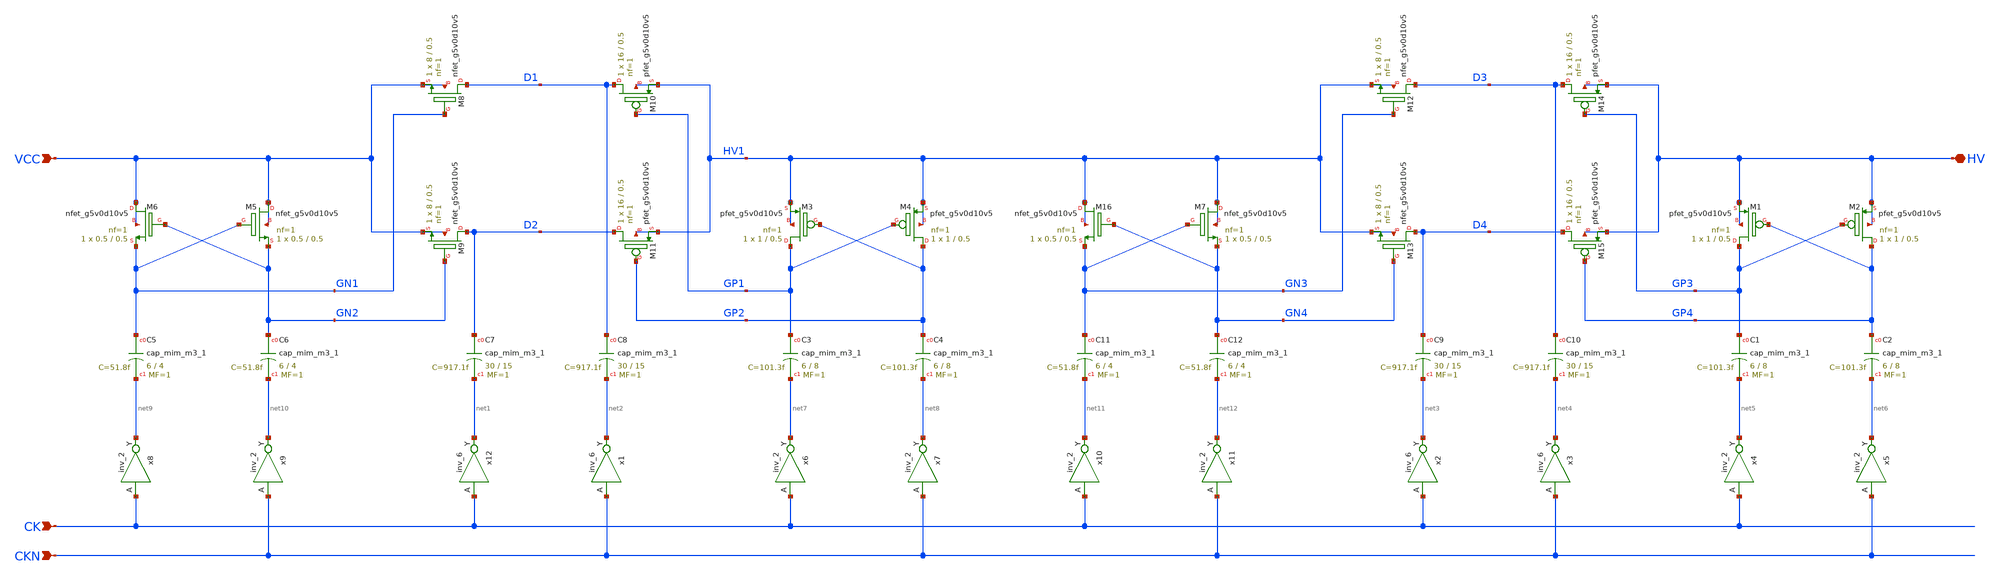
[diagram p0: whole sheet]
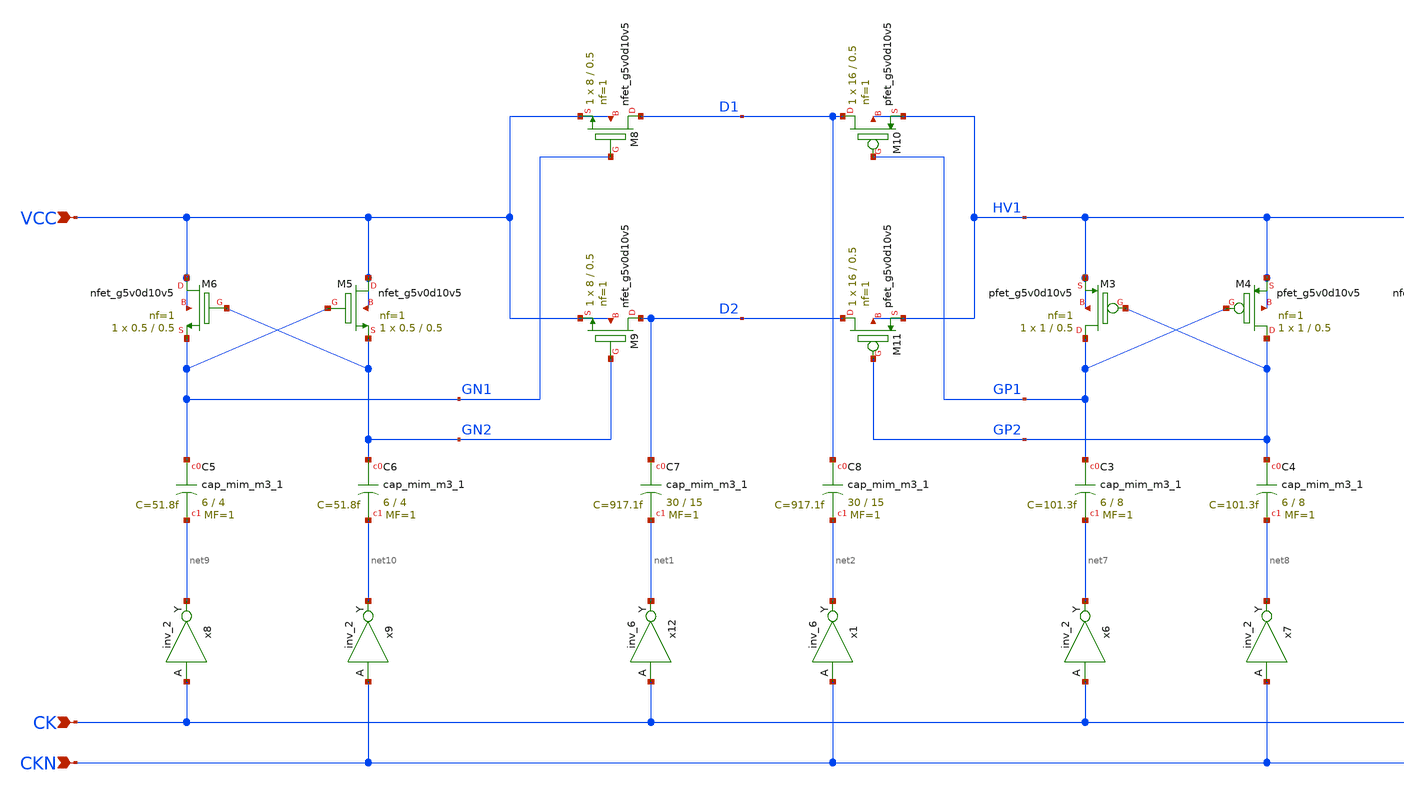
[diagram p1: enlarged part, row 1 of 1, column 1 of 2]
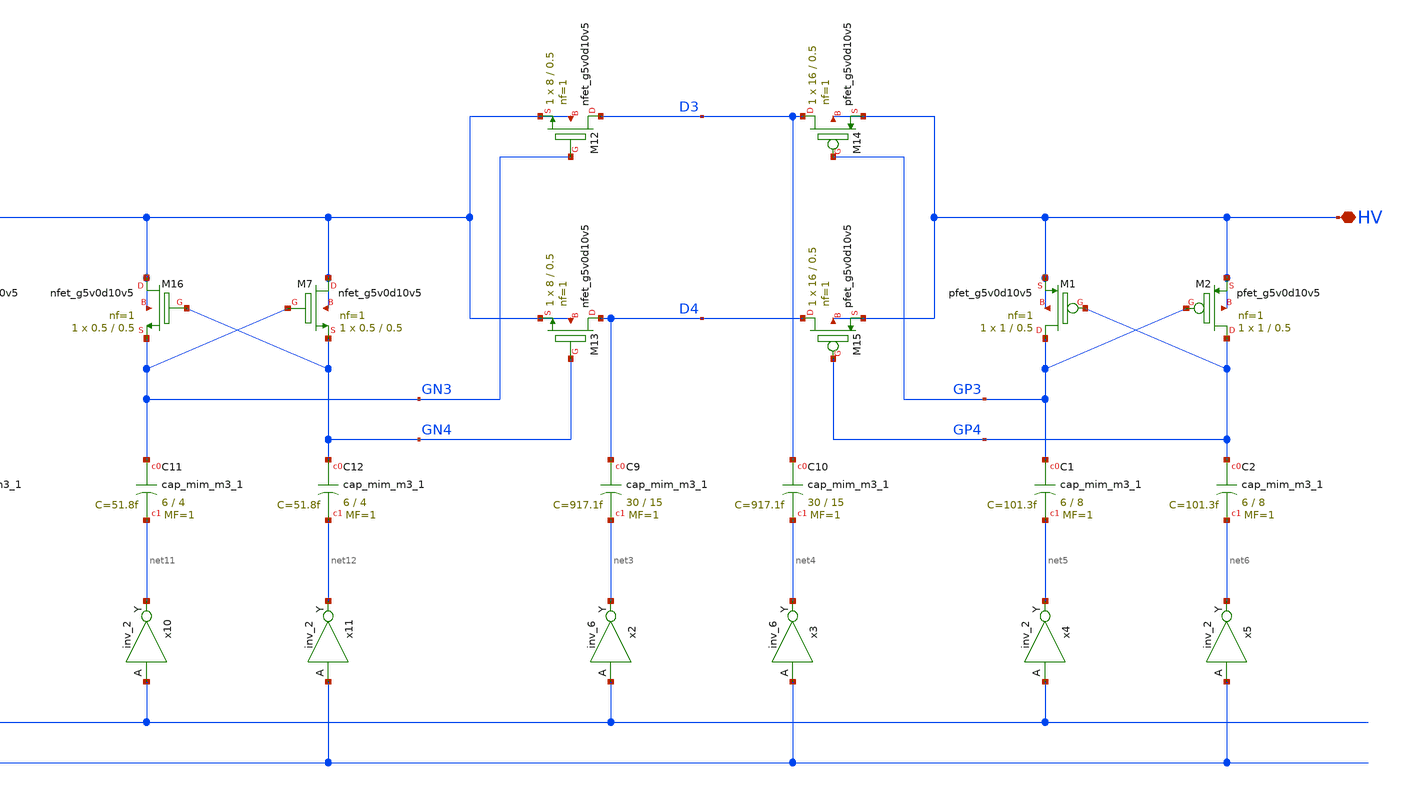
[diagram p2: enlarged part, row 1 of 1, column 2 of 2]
** sch_path: sky130A/xschem_libs/sky130_tests_ase/charge_pump2/schematic/charge_pump2.sch
* Copyright 2021 Stefan Frederik Schippers
* Licensed under the Apache License, Version 2.0 (the "License");
* you may not use this file except in compliance with the License.
* You may obtain a copy of the License at
* https://www.apache.org/licenses/LICENSE-2.0
* Unless required by applicable law or agreed to in writing, software
* distributed under the License is distributed on an "AS IS" BASIS,
* WITHOUT WARRANTIES OR CONDITIONS OF ANY KIND, either express or implied.
* See the License for the specific language governing permissions and
* limitations under the License.
**.subckt charge_pump2 VCC HV CK CKN
*.ipin VCC
*.iopin HV
*.ipin CK
*.ipin CKN
XM8 D1 GN1 VCC VCC sky130_fd_pr__nfet_g5v0d10v5 L=0.5 W=8 nf=1 ad='int((1 + 1)/2) * 8 / 1 * 0.29' as='int((1 + 2)/2) * 8 / 1 * 0.29'
+ pd='2*int((1 + 1)/2) * (8 / 1 + 0.29)' ps='2*int((1 + 2)/2) * (8 / 1 + 0.29)' nrd='0.29 / 8 ' nrs='0.29 / 8 '
+ sa=0 sb=0 sd=0 mult=1 m=1
XM9 D2 GN2 VCC VCC sky130_fd_pr__nfet_g5v0d10v5 L=0.5 W=8 nf=1 ad='int((1 + 1)/2) * 8 / 1 * 0.29' as='int((1 + 2)/2) * 8 / 1 * 0.29'
+ pd='2*int((1 + 1)/2) * (8 / 1 + 0.29)' ps='2*int((1 + 2)/2) * (8 / 1 + 0.29)' nrd='0.29 / 8 ' nrs='0.29 / 8 '
+ sa=0 sb=0 sd=0 mult=1 m=1
XM10 D1 GP1 HV1 HV1 sky130_fd_pr__pfet_g5v0d10v5 L=0.5 W=16 nf=1 ad='int((1 + 1)/2) * 16 / 1 * 0.29'
+ as='int((1 + 2)/2) * 16 / 1 * 0.29' pd='2*int((1 + 1)/2) * (16 / 1 + 0.29)' ps='2*int((1 + 2)/2) * (16 / 1 + 0.29)'
+ nrd='0.29 / 16 ' nrs='0.29 / 16 ' sa=0 sb=0 sd=0 mult=1 m=1
XM11 D2 GP2 HV1 HV1 sky130_fd_pr__pfet_g5v0d10v5 L=0.5 W=16 nf=1 ad='int((1 + 1)/2) * 16 / 1 * 0.29'
+ as='int((1 + 2)/2) * 16 / 1 * 0.29' pd='2*int((1 + 1)/2) * (16 / 1 + 0.29)' ps='2*int((1 + 2)/2) * (16 / 1 + 0.29)'
+ nrd='0.29 / 16 ' nrs='0.29 / 16 ' sa=0 sb=0 sd=0 mult=1 m=1
XC7 D2 net1 sky130_fd_pr__cap_mim_m3_1 W=30 L=15 MF=1 m=1
XC8 D1 net2 sky130_fd_pr__cap_mim_m3_1 W=30 L=15 MF=1 m=1
XM12 D3 GN3 HV1 HV1 sky130_fd_pr__nfet_g5v0d10v5 L=0.5 W=8 nf=1 ad='int((1 + 1)/2) * 8 / 1 * 0.29' as='int((1 + 2)/2) * 8 / 1 * 0.29'
+ pd='2*int((1 + 1)/2) * (8 / 1 + 0.29)' ps='2*int((1 + 2)/2) * (8 / 1 + 0.29)' nrd='0.29 / 8 ' nrs='0.29 / 8 '
+ sa=0 sb=0 sd=0 mult=1 m=1
XM13 D4 GN4 HV1 HV1 sky130_fd_pr__nfet_g5v0d10v5 L=0.5 W=8 nf=1 ad='int((1 + 1)/2) * 8 / 1 * 0.29' as='int((1 + 2)/2) * 8 / 1 * 0.29'
+ pd='2*int((1 + 1)/2) * (8 / 1 + 0.29)' ps='2*int((1 + 2)/2) * (8 / 1 + 0.29)' nrd='0.29 / 8 ' nrs='0.29 / 8 '
+ sa=0 sb=0 sd=0 mult=1 m=1
XM14 D3 GP3 HV HV sky130_fd_pr__pfet_g5v0d10v5 L=0.5 W=16 nf=1 ad='int((1 + 1)/2) * 16 / 1 * 0.29' as='int((1 + 2)/2) * 16 / 1 * 0.29'
+ pd='2*int((1 + 1)/2) * (16 / 1 + 0.29)' ps='2*int((1 + 2)/2) * (16 / 1 + 0.29)' nrd='0.29 / 16 ' nrs='0.29 / 16 '
+ sa=0 sb=0 sd=0 mult=1 m=1
XM15 D4 GP4 HV HV sky130_fd_pr__pfet_g5v0d10v5 L=0.5 W=16 nf=1 ad='int((1 + 1)/2) * 16 / 1 * 0.29' as='int((1 + 2)/2) * 16 / 1 * 0.29'
+ pd='2*int((1 + 1)/2) * (16 / 1 + 0.29)' ps='2*int((1 + 2)/2) * (16 / 1 + 0.29)' nrd='0.29 / 16 ' nrs='0.29 / 16 '
+ sa=0 sb=0 sd=0 mult=1 m=1
XC9 D4 net3 sky130_fd_pr__cap_mim_m3_1 W=30 L=15 MF=1 m=1
XC10 D3 net4 sky130_fd_pr__cap_mim_m3_1 W=30 L=15 MF=1 m=1
x12 CK GND GND VCC VCC net1 sky130_fd_sc_hd__inv_6
x1 CKN GND GND VCC VCC net2 sky130_fd_sc_hd__inv_6
x2 CK GND GND VCC VCC net3 sky130_fd_sc_hd__inv_6
x3 CKN GND GND VCC VCC net4 sky130_fd_sc_hd__inv_6
XM1 GP3 GP4 HV HV sky130_fd_pr__pfet_g5v0d10v5 L=0.5 W=1 nf=1 ad='int((1 + 1)/2) * 1 / 1 * 0.29' as='int((1 + 2)/2) * 1 / 1 * 0.29'
+ pd='2*int((1 + 1)/2) * (1 / 1 + 0.29)' ps='2*int((1 + 2)/2) * (1 / 1 + 0.29)' nrd='0.29 / 1 ' nrs='0.29 / 1 '
+ sa=0 sb=0 sd=0 mult=1 m=1
XM2 GP4 GP3 HV HV sky130_fd_pr__pfet_g5v0d10v5 L=0.5 W=1 nf=1 ad='int((1 + 1)/2) * 1 / 1 * 0.29' as='int((1 + 2)/2) * 1 / 1 * 0.29'
+ pd='2*int((1 + 1)/2) * (1 / 1 + 0.29)' ps='2*int((1 + 2)/2) * (1 / 1 + 0.29)' nrd='0.29 / 1 ' nrs='0.29 / 1 '
+ sa=0 sb=0 sd=0 mult=1 m=1
XC1 GP3 net5 sky130_fd_pr__cap_mim_m3_1 W=6 L=8 MF=1 m=1
XC2 GP4 net6 sky130_fd_pr__cap_mim_m3_1 W=6 L=8 MF=1 m=1
XM3 GP1 GP2 HV1 HV1 sky130_fd_pr__pfet_g5v0d10v5 L=0.5 W=1 nf=1 ad='int((1 + 1)/2) * 1 / 1 * 0.29' as='int((1 + 2)/2) * 1 / 1 * 0.29'
+ pd='2*int((1 + 1)/2) * (1 / 1 + 0.29)' ps='2*int((1 + 2)/2) * (1 / 1 + 0.29)' nrd='0.29 / 1 ' nrs='0.29 / 1 '
+ sa=0 sb=0 sd=0 mult=1 m=1
XM4 GP2 GP1 HV1 HV1 sky130_fd_pr__pfet_g5v0d10v5 L=0.5 W=1 nf=1 ad='int((1 + 1)/2) * 1 / 1 * 0.29' as='int((1 + 2)/2) * 1 / 1 * 0.29'
+ pd='2*int((1 + 1)/2) * (1 / 1 + 0.29)' ps='2*int((1 + 2)/2) * (1 / 1 + 0.29)' nrd='0.29 / 1 ' nrs='0.29 / 1 '
+ sa=0 sb=0 sd=0 mult=1 m=1
XC3 GP1 net7 sky130_fd_pr__cap_mim_m3_1 W=6 L=8 MF=1 m=1
XC4 GP2 net8 sky130_fd_pr__cap_mim_m3_1 W=6 L=8 MF=1 m=1
x4 CK GND GND VCC VCC net5 sky130_fd_sc_hd__inv_2
x5 CKN GND GND VCC VCC net6 sky130_fd_sc_hd__inv_2
x6 CK GND GND VCC VCC net7 sky130_fd_sc_hd__inv_2
x7 CKN GND GND VCC VCC net8 sky130_fd_sc_hd__inv_2
XC5 GN1 net9 sky130_fd_pr__cap_mim_m3_1 W=6 L=4 MF=1 m=1
XC6 GN2 net10 sky130_fd_pr__cap_mim_m3_1 W=6 L=4 MF=1 m=1
x8 CK GND GND VCC VCC net9 sky130_fd_sc_hd__inv_2
x9 CKN GND GND VCC VCC net10 sky130_fd_sc_hd__inv_2
XM5 VCC GN1 GN2 VCC sky130_fd_pr__nfet_g5v0d10v5 L=0.5 W=0.5 nf=1 ad='int((1 + 1)/2) * 0.5 / 1 * 0.29'
+ as='int((1 + 2)/2) * 0.5 / 1 * 0.29' pd='2*int((1 + 1)/2) * (0.5 / 1 + 0.29)' ps='2*int((1 + 2)/2) * (0.5 / 1 + 0.29)'
+ nrd='0.29 / 0.5 ' nrs='0.29 / 0.5 ' sa=0 sb=0 sd=0 mult=1 m=1
XM6 VCC GN2 GN1 VCC sky130_fd_pr__nfet_g5v0d10v5 L=0.5 W=0.5 nf=1 ad='int((1 + 1)/2) * 0.5 / 1 * 0.29'
+ as='int((1 + 2)/2) * 0.5 / 1 * 0.29' pd='2*int((1 + 1)/2) * (0.5 / 1 + 0.29)' ps='2*int((1 + 2)/2) * (0.5 / 1 + 0.29)'
+ nrd='0.29 / 0.5 ' nrs='0.29 / 0.5 ' sa=0 sb=0 sd=0 mult=1 m=1
XC11 GN3 net11 sky130_fd_pr__cap_mim_m3_1 W=6 L=4 MF=1 m=1
XC12 GN4 net12 sky130_fd_pr__cap_mim_m3_1 W=6 L=4 MF=1 m=1
x10 CK GND GND VCC VCC net11 sky130_fd_sc_hd__inv_2
x11 CKN GND GND VCC VCC net12 sky130_fd_sc_hd__inv_2
XM7 HV1 GN3 GN4 HV1 sky130_fd_pr__nfet_g5v0d10v5 L=0.5 W=0.5 nf=1 ad='int((1 + 1)/2) * 0.5 / 1 * 0.29'
+ as='int((1 + 2)/2) * 0.5 / 1 * 0.29' pd='2*int((1 + 1)/2) * (0.5 / 1 + 0.29)' ps='2*int((1 + 2)/2) * (0.5 / 1 + 0.29)'
+ nrd='0.29 / 0.5 ' nrs='0.29 / 0.5 ' sa=0 sb=0 sd=0 mult=1 m=1
XM16 HV1 GN4 GN3 HV1 sky130_fd_pr__nfet_g5v0d10v5 L=0.5 W=0.5 nf=1 ad='int((1 + 1)/2) * 0.5 / 1 * 0.29'
+ as='int((1 + 2)/2) * 0.5 / 1 * 0.29' pd='2*int((1 + 1)/2) * (0.5 / 1 + 0.29)' ps='2*int((1 + 2)/2) * (0.5 / 1 + 0.29)'
+ nrd='0.29 / 0.5 ' nrs='0.29 / 0.5 ' sa=0 sb=0 sd=0 mult=1 m=1
**.ends
.end
